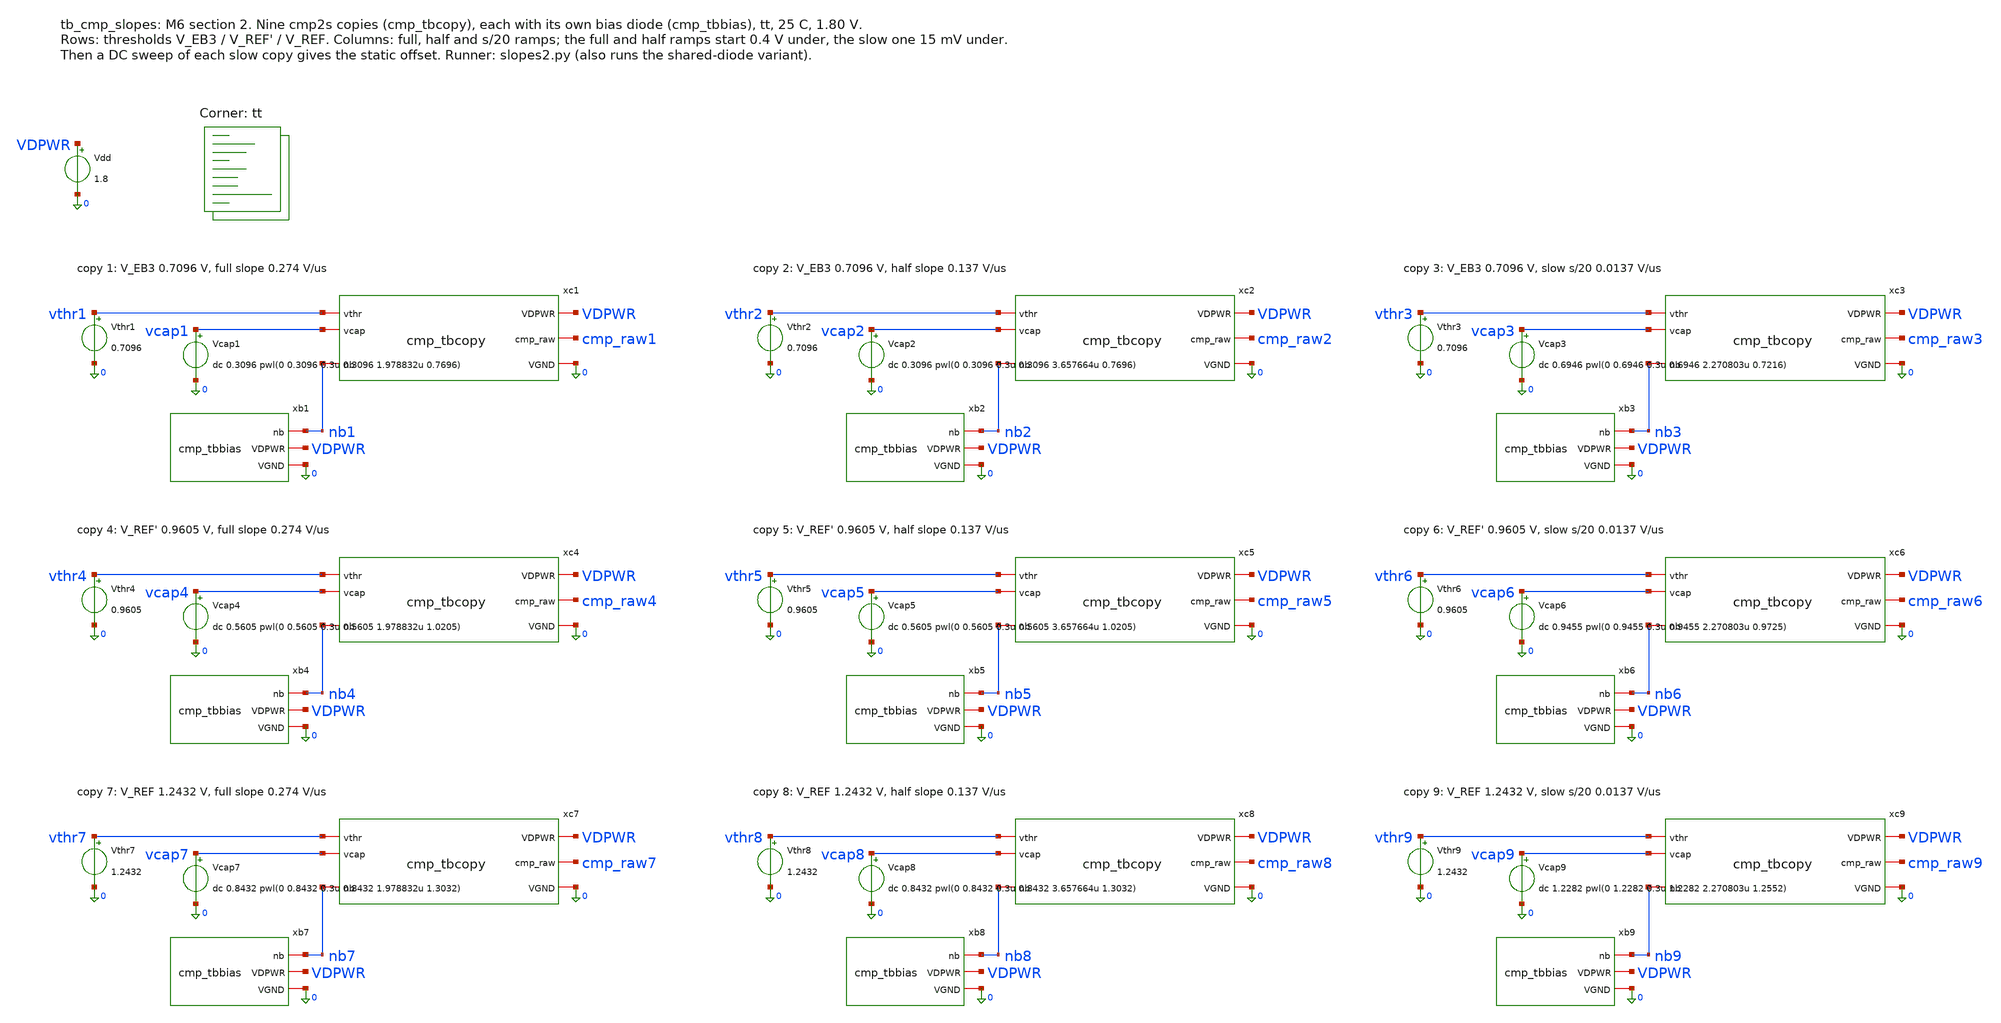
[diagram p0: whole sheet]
** sch_path: xschem/tb_cmp_slopes.sch
**.subckt tb_cmp_slopes
xc1 vthr1 vcap1 nb1 VDPWR cmp_raw1 0 cmp_tbcopy
xb1 nb1 VDPWR 0 cmp_tbbias
Vthr1 vthr1 0 0.7096
Vcap1 vcap1 0 dc 0.3096 pwl(0 0.3096 0.3u 0.3096 1.978832u 0.7696)
xc2 vthr2 vcap2 nb2 VDPWR cmp_raw2 0 cmp_tbcopy
xb2 nb2 VDPWR 0 cmp_tbbias
Vthr2 vthr2 0 0.7096
Vcap2 vcap2 0 dc 0.3096 pwl(0 0.3096 0.3u 0.3096 3.657664u 0.7696)
xc3 vthr3 vcap3 nb3 VDPWR cmp_raw3 0 cmp_tbcopy
xb3 nb3 VDPWR 0 cmp_tbbias
Vthr3 vthr3 0 0.7096
Vcap3 vcap3 0 dc 0.6946 pwl(0 0.6946 0.3u 0.6946 2.270803u 0.7216)
xc4 vthr4 vcap4 nb4 VDPWR cmp_raw4 0 cmp_tbcopy
xb4 nb4 VDPWR 0 cmp_tbbias
Vthr4 vthr4 0 0.9605
Vcap4 vcap4 0 dc 0.5605 pwl(0 0.5605 0.3u 0.5605 1.978832u 1.0205)
xc5 vthr5 vcap5 nb5 VDPWR cmp_raw5 0 cmp_tbcopy
xb5 nb5 VDPWR 0 cmp_tbbias
Vthr5 vthr5 0 0.9605
Vcap5 vcap5 0 dc 0.5605 pwl(0 0.5605 0.3u 0.5605 3.657664u 1.0205)
xc6 vthr6 vcap6 nb6 VDPWR cmp_raw6 0 cmp_tbcopy
xb6 nb6 VDPWR 0 cmp_tbbias
Vthr6 vthr6 0 0.9605
Vcap6 vcap6 0 dc 0.9455 pwl(0 0.9455 0.3u 0.9455 2.270803u 0.9725)
xc7 vthr7 vcap7 nb7 VDPWR cmp_raw7 0 cmp_tbcopy
xb7 nb7 VDPWR 0 cmp_tbbias
Vthr7 vthr7 0 1.2432
Vcap7 vcap7 0 dc 0.8432 pwl(0 0.8432 0.3u 0.8432 1.978832u 1.3032)
xc8 vthr8 vcap8 nb8 VDPWR cmp_raw8 0 cmp_tbcopy
xb8 nb8 VDPWR 0 cmp_tbbias
Vthr8 vthr8 0 1.2432
Vcap8 vcap8 0 dc 0.8432 pwl(0 0.8432 0.3u 0.8432 3.657664u 1.3032)
xc9 vthr9 vcap9 nb9 VDPWR cmp_raw9 0 cmp_tbcopy
xb9 nb9 VDPWR 0 cmp_tbbias
Vthr9 vthr9 0 1.2432
Vcap9 vcap9 0 dc 1.2282 pwl(0 1.2282 0.3u 1.2282 2.270803u 1.2552)
Vdd VDPWR 0 1.8
**** begin user architecture code

.include /foss/pdks/sky130A/libs.ref/sky130_fd_sc_hd/spice/sky130_fd_sc_hd.spice
.option method=gear
.temp 25
.control
tran 0.2n 3.85u 0 0.2n
meas tran to1 when v(cmp_raw1)=0.9 rise=1
meas tran to2 when v(cmp_raw2)=0.9 rise=1
meas tran to3 when v(cmp_raw3)=0.9 rise=1
meas tran to4 when v(cmp_raw4)=0.9 rise=1
meas tran to5 when v(cmp_raw5)=0.9 rise=1
meas tran to6 when v(cmp_raw6)=0.9 rise=1
meas tran to7 when v(cmp_raw7)=0.9 rise=1
meas tran to8 when v(cmp_raw8)=0.9 rise=1
meas tran to9 when v(cmp_raw9)=0.9 rise=1
meas tran nb0 find v(nb1) at=0.9u
meas tran nbmax max v(nb1) from=1u to=3.85u
meas tran nbmin min v(nb1) from=1u to=3.85u
echo RESULT to1=$&to1 to2=$&to2 to3=$&to3 to4=$&to4 to5=$&to5 to6=$&to6 to7=$&to7 to8=$&to8
+ to9=$&to9 nb0=$&nb0 nbmax=$&nbmax nbmin=$&nbmin
* static offset: DC sweep of each slow copy's vcap across its threshold (5 uV steps)
dc vcap3 0.7046 0.7146 5u
meas dc trip3 when v(cmp_raw3)=0.9 rise=1
echo RESULT trip3=$&trip3
dc vcap6 0.9555 0.9655 5u
meas dc trip6 when v(cmp_raw6)=0.9 rise=1
echo RESULT trip6=$&trip6
dc vcap9 1.2382 1.2482 5u
meas dc trip9 when v(cmp_raw9)=0.9 rise=1
echo RESULT trip9=$&trip9
.endc

.lib $::SKYWATER_MODELS/sky130.lib.spice tt
**** end user architecture code
**.ends

* expanding   symbol:  cmp_tbcopy.sym # of pins=6
** sym_path: xschem/cmp_tbcopy.sym
** sch_path: xschem/cmp_tbcopy.sch
.subckt cmp_tbcopy vthr vcap nb VDPWR cmp_raw VGND
*.ipin vthr
*.ipin vcap
*.iopin nb
*.iopin VDPWR
*.opin cmp_raw
*.iopin VGND
x1 vthr vcap ib_cmp1 ib_cmp2 VDPWR cmp_raw VGND cmp2s
XMNB3 ib_cmp1 nb VGND VGND sky130_fd_pr__nfet_01v8 L=8 W=4 nf=1 ad='int((1 + 1)/2) * 4 / 1 * 0.29' as='int((1
+ + 2)/2) * 4 / 1 * 0.29' pd='2*int((1 + 1)/2) * (4 / 1 + 0.29)' ps='2*int((1 + 2)/2) * (4 / 1 + 0.29)' nrd='0.29
+ / 4 ' nrs='0.29 / 4 ' sa=0 sb=0 sd=0 mult=4 m=4
XMNB4 ib_cmp2 nb VGND VGND sky130_fd_pr__nfet_01v8 L=8 W=4 nf=1 ad='int((1 + 1)/2) * 4 / 1 * 0.29' as='int((1
+ + 2)/2) * 4 / 1 * 0.29' pd='2*int((1 + 1)/2) * (4 / 1 + 0.29)' ps='2*int((1 + 2)/2) * (4 / 1 + 0.29)' nrd='0.29
+ / 4 ' nrs='0.29 / 4 ' sa=0 sb=0 sd=0 mult=4 m=4
Cw1 ib_cmp1 VGND 40f m=1
Cw2 ib_cmp2 VGND 40f m=1
.ends


* expanding   symbol:  cmp_tbbias.sym # of pins=3
** sym_path: xschem/cmp_tbbias.sym
** sch_path: xschem/cmp_tbbias.sch
.subckt cmp_tbbias nb VDPWR VGND
*.iopin VDPWR
*.iopin nb
*.iopin VGND
Iref VDPWR nb 1.386u
XMNB1 nb nb VGND VGND sky130_fd_pr__nfet_01v8 L=8 W=4 nf=1 ad='int((1 + 1)/2) * 4 / 1 * 0.29' as='int((1
+ + 2)/2) * 4 / 1 * 0.29' pd='2*int((1 + 1)/2) * (4 / 1 + 0.29)' ps='2*int((1 + 2)/2) * (4 / 1 + 0.29)' nrd='0.29
+ / 4 ' nrs='0.29 / 4 ' sa=0 sb=0 sd=0 mult=1 m=1
.ends


* expanding   symbol:  cmp2s.sym # of pins=7
** sym_path: xschem/cmp2s.sym
** sch_path: xschem/cmp2s.sch
.subckt cmp2s vthr vcap ib_cmp1 ib_cmp2 VDPWR cmp_raw VGND
*.iopin VDPWR
*.iopin VGND
*.ipin vthr
*.ipin vcap
*.iopin ib_cmp1
*.iopin ib_cmp2
*.opin cmp_raw
XM2a nd nd VDPWR VDPWR sky130_fd_pr__pfet_01v8_lvt L=4 W=4 nf=1 ad='int((1 + 1)/2) * 4 / 1 * 0.29' as='int((1
+ + 2)/2) * 4 / 1 * 0.29' pd='2*int((1 + 1)/2) * (4 / 1 + 0.29)' ps='2*int((1 + 2)/2) * (4 / 1 + 0.29)' nrd='0.29
+ / 4 ' nrs='0.29 / 4 ' sa=0 sb=0 sd=0 mult=8 m=8
XM2b n1 nd VDPWR VDPWR sky130_fd_pr__pfet_01v8_lvt L=4 W=4 nf=1 ad='int((1 + 1)/2) * 4 / 1 * 0.29' as='int((1
+ + 2)/2) * 4 / 1 * 0.29' pd='2*int((1 + 1)/2) * (4 / 1 + 0.29)' ps='2*int((1 + 2)/2) * (4 / 1 + 0.29)' nrd='0.29
+ / 4 ' nrs='0.29 / 4 ' sa=0 sb=0 sd=0 mult=8 m=8
XM1a nd vthr ib_cmp1 VGND sky130_fd_pr__nfet_01v8_lvt L=1.75 W=10 nf=1 ad='int((1 + 1)/2) * 10 / 1 *
+ 0.29' as='int((1 + 2)/2) * 10 / 1 * 0.29' pd='2*int((1 + 1)/2) * (10 / 1 + 0.29)' ps='2*int((1 + 2)/2)
+ * (10 / 1 + 0.29)' nrd='0.29 / 10 ' nrs='0.29 / 10 ' sa=0 sb=0 sd=0 mult=6 m=6
XM1b n1 vcap ib_cmp1 VGND sky130_fd_pr__nfet_01v8_lvt L=1.75 W=10 nf=1 ad='int((1 + 1)/2) * 10 / 1 *
+ 0.29' as='int((1 + 2)/2) * 10 / 1 * 0.29' pd='2*int((1 + 1)/2) * (10 / 1 + 0.29)' ps='2*int((1 + 2)/2)
+ * (10 / 1 + 0.29)' nrd='0.29 / 10 ' nrs='0.29 / 10 ' sa=0 sb=0 sd=0 mult=6 m=6
XM3 ib_cmp2 n1 VDPWR VDPWR sky130_fd_pr__pfet_01v8_lvt L=1 W=4 nf=1 ad='int((1 + 1)/2) * 4 / 1 * 0.29' as='int((1
+ + 2)/2) * 4 / 1 * 0.29' pd='2*int((1 + 1)/2) * (4 / 1 + 0.29)' ps='2*int((1 + 2)/2) * (4 / 1 + 0.29)' nrd='0.29
+ / 4 ' nrs='0.29 / 4 ' sa=0 sb=0 sd=0 mult=3 m=3
XMIP x ib_cmp2 VDPWR VDPWR sky130_fd_pr__pfet_01v8 L=1 W=0.42 nf=1 ad='int((1 + 1)/2) * 0.42 / 1 * 0.29' as='int((1
+ + 2)/2) * 0.42 / 1 * 0.29' pd='2*int((1 + 1)/2) * (0.42 / 1 + 0.29)' ps='2*int((1 + 2)/2) * (0.42 / 1
+ + 0.29)' nrd='0.29 / 0.42 ' nrs='0.29 / 0.42 ' sa=0 sb=0 sd=0 mult=1 m=1
XMIN x ib_cmp2 VGND VGND sky130_fd_pr__nfet_01v8 L=0.15 W=2 nf=1 ad='int((1 + 1)/2) * 2 / 1 * 0.29' as='int((1
+ + 2)/2) * 2 / 1 * 0.29' pd='2*int((1 + 1)/2) * (2 / 1 + 0.29)' ps='2*int((1 + 2)/2) * (2 / 1 + 0.29)' nrd='0.29
+ / 2 ' nrs='0.29 / 2 ' sa=0 sb=0 sd=0 mult=1 m=1
xinv x VGND VGND VDPWR VDPWR cmp_raw sky130_fd_sc_hd__inv_1
.ends

.end
